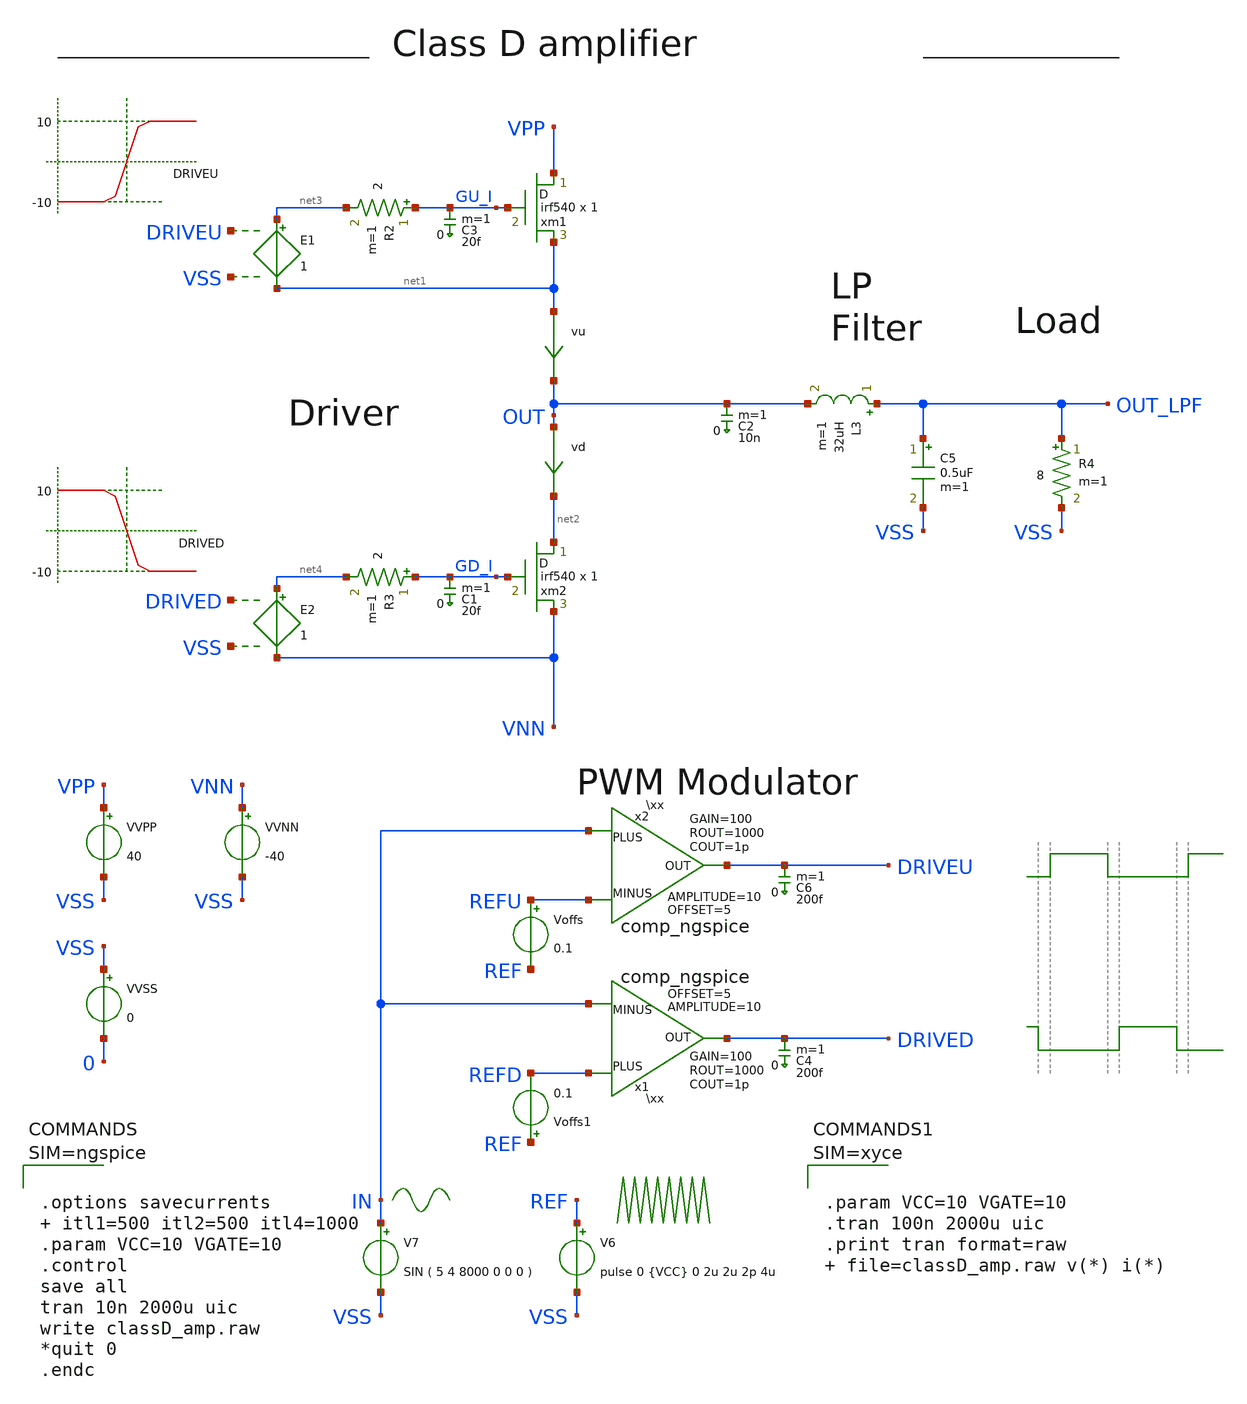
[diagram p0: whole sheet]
** sch_path: xschem_library/examples/classD_amp.sch
* Copyright (C) 1998-2026 Stefan Frederik Schippers
* This program is free software; you can redistribute it and/or modify
* it under the terms of the GNU General Public License as published by
* the Free Software Foundation; either version 2 of the License, or
* (at your option) any later version.
* This program is distributed in the hope that it will be useful,
* but WITHOUT ANY WARRANTY; without even the implied warranty of
* MERCHANTABILITY or FITNESS FOR A PARTICULAR PURPOSE.  See the
* GNU General Public License for more details.
* You should have received a copy of the GNU General Public License
* along with this program; if not, write to the Free Software
**.subckt classD_amp
xm2 net2 GD_I VNN irf540 m=1
xm1 VPP GU_I net1 irf540 m=1
vd OUT net2 0
.save i(vd)
vu net1 OUT 0
.save i(vu)
x1 REFD DRIVED IN comp_ngspice OFFSET=5 AMPLITUDE=10 GAIN=100 ROUT=1000 COUT=1p
VVPP VPP VSS 40
VVNN VNN VSS -40
VVSS VSS 0 0
R2 GU_I net3 2 m=1
R3 GD_I net4 2 m=1
C3 GU_I 0 20f m=1
C1 GD_I 0 20f m=1
C2 OUT 0 10n m=1
V6 REF VSS pulse 0 {VCC} 0 2u 2u 2p 4u
V7 IN VSS SIN ( 5 4 8000 0 0 0 )
C4 DRIVED 0 200f m=1
L3 OUT_LPF OUT 32uH m=1
C5 OUT_LPF VSS 0.5uF m=1
R4 OUT_LPF VSS 8 m=1
x2 IN DRIVEU REFU comp_ngspice OFFSET=5 AMPLITUDE=10 GAIN=100 ROUT=1000 COUT=1p
C6 DRIVEU 0 200f m=1
Voffs REFU REF 0.1
Voffs1 REF REFD 0.1
E1 net3 net1 DRIVEU VSS 1
E2 net4 VNN DRIVED VSS 1
**** begin user architecture code



.options savecurrents  itl1=500 itl2=500 itl4=1000
.param VCC=10 VGATE=10
.control
save all
tran 10n 2000u uic
write classD_amp.raw
*quit 0
.endc






**** end user architecture code
**.ends

* expanding   symbol:  comp_ngspice.sym # of pins=3
** sym_path: xschem_library/ngspice/comp_ngspice.sym
** sch_path: xschem_library/ngspice/comp_ngspice.sch
.subckt comp_ngspice PLUS OUT MINUS  OFFSET=0 AMPLITUDE=5 GAIN=100 ROUT=1000 COUT=1p
*.ipin PLUS
*.ipin MINUS
*.opin OUT
B1 IOUT 0 V = {OFFSET + AMPLITUDE/2*(tanh(V(IPLUS,IMINUS)*GAIN*2/AMPLITUDE))}
R1 OUT IOUT {ROUT} m=1
C3 OUT 0 {COUT} m=1
V1 IPLUS PLUS 0
V2 IMINUS MINUS 0
.ends

**** begin user architecture code
.SUBCKT irf540 1 2 3
M1 9 7 8 8 MM L=100u W=100u
* Default values used in MM:
* The voltage-dependent capacitances are
* not included. Other default values are:
* RS=0 RD=0 LD=0 CBD=0 CBS=0 CGBO=0
.MODEL MM NMOS LEVEL=1 IS=1e-32 VTO=3.56362 LAMBDA=0.00291031 KP=25.0081 CGSO=1.60584e-05
+ CGDO=4.25919e-07
RS 8 3 0.0317085
D1 3 1 MD
.MODEL MD D IS=1.02194e-10 RS=0.00968022 N=1.21527 BV=100 IBV=0.00025 EG=1.2 XTI=3.03885 TT=1e-07
+ CJO=1.81859e-09 VJ=1.1279 M=0.449161 FC=0.5
RDS 3 1 4e+06
RD 9 1 0.0135649
RG 2 7 5.11362
D2 4 5 MD1
* Default values used in MD1:
* RS=0 EG=1.11 XTI=3.0 TT=0
* BV=infinite IBV=1mA
.MODEL MD1 D IS=1e-32 N=50 CJO=2.49697e-09 VJ=0.5 M=0.9 FC=1e-08
D3 0 5 MD2
* Default values used in MD2:
* EG=1.11 XTI=3.0 TT=0 CJO=0
* BV=infinite IBV=1mA
.MODEL MD2 D IS=1e-10 N=0.4 RS=3e-06
RL 5 10 1
FI2 7 9 VFI2 -1
VFI2 4 0 0
EV16 10 0 9 7 1
CAP 11 10 2.49697e-09
FI1 7 9 VFI1 -1
VFI1 11 6 0
RCAP 6 10 1
D4 0 6 MD3
* Default values used in MD3:
* EG=1.11 XTI=3.0 TT=0 CJO=0
* RS=0 BV=infinite IBV=1mA
.MODEL MD3 D IS=1e-10 N=0.4
.ENDS

**** end user architecture code
.end
